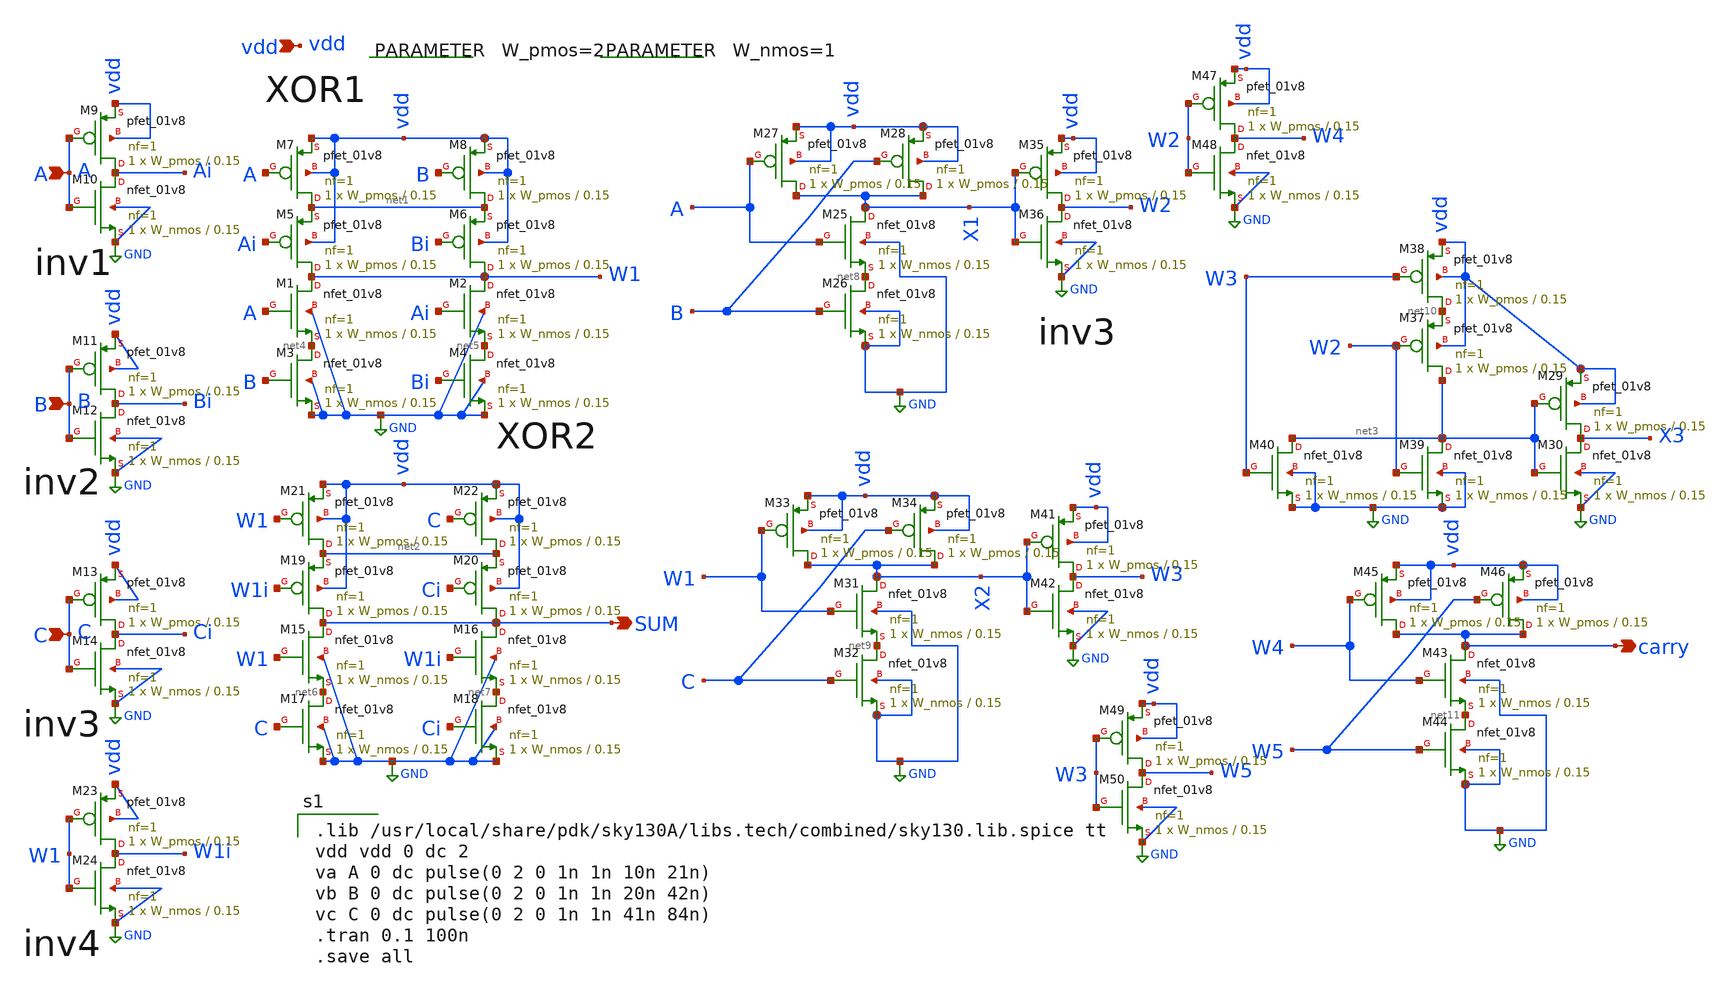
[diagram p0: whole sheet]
** sch_path: Circuit Files/circuits/circuits/FA_mos_realization.sch
**.subckt FA_mos_realization A B vdd C SUM carry
*.ipin A
*.ipin B
*.ipin vdd
*.ipin C
*.opin SUM
*.opin carry
XM1 W1 A net4 GND sky130_fd_pr__nfet_01v8 L=0.15 W=W_nmos nf=1 ad='int((nf+1)/2) * W/nf * 0.29' as='int((nf+2)/2) * W/nf * 0.29'
+ pd='2*int((nf+1)/2) * (W/nf + 0.29)' ps='2*int((nf+2)/2) * (W/nf + 0.29)' nrd='0.29 / W' nrs='0.29 / W'
+ sa=0 sb=0 sd=0 mult=1 m=1
XM2 W1 Ai net5 GND sky130_fd_pr__nfet_01v8 L=0.15 W=W_nmos nf=1 ad='int((nf+1)/2) * W/nf * 0.29' as='int((nf+2)/2) * W/nf * 0.29'
+ pd='2*int((nf+1)/2) * (W/nf + 0.29)' ps='2*int((nf+2)/2) * (W/nf + 0.29)' nrd='0.29 / W' nrs='0.29 / W'
+ sa=0 sb=0 sd=0 mult=1 m=1
XM3 net4 B GND GND sky130_fd_pr__nfet_01v8 L=0.15 W=W_nmos nf=1 ad='int((nf+1)/2) * W/nf * 0.29' as='int((nf+2)/2) * W/nf * 0.29'
+ pd='2*int((nf+1)/2) * (W/nf + 0.29)' ps='2*int((nf+2)/2) * (W/nf + 0.29)' nrd='0.29 / W' nrs='0.29 / W'
+ sa=0 sb=0 sd=0 mult=1 m=1
XM4 net5 Bi GND GND sky130_fd_pr__nfet_01v8 L=0.15 W=W_nmos nf=1 ad='int((nf+1)/2) * W/nf * 0.29' as='int((nf+2)/2) * W/nf * 0.29'
+ pd='2*int((nf+1)/2) * (W/nf + 0.29)' ps='2*int((nf+2)/2) * (W/nf + 0.29)' nrd='0.29 / W' nrs='0.29 / W'
+ sa=0 sb=0 sd=0 mult=1 m=1
XM5 W1 Ai net1 vdd sky130_fd_pr__pfet_01v8 L=0.15 W=W_pmos nf=1 ad='int((nf+1)/2) * W/nf * 0.29' as='int((nf+2)/2) * W/nf * 0.29'
+ pd='2*int((nf+1)/2) * (W/nf + 0.29)' ps='2*int((nf+2)/2) * (W/nf + 0.29)' nrd='0.29 / W' nrs='0.29 / W'
+ sa=0 sb=0 sd=0 mult=1 m=1
XM6 W1 Bi net1 vdd sky130_fd_pr__pfet_01v8 L=0.15 W=W_pmos nf=1 ad='int((nf+1)/2) * W/nf * 0.29' as='int((nf+2)/2) * W/nf * 0.29'
+ pd='2*int((nf+1)/2) * (W/nf + 0.29)' ps='2*int((nf+2)/2) * (W/nf + 0.29)' nrd='0.29 / W' nrs='0.29 / W'
+ sa=0 sb=0 sd=0 mult=1 m=1
XM7 net1 A vdd vdd sky130_fd_pr__pfet_01v8 L=0.15 W=W_pmos nf=1 ad='int((nf+1)/2) * W/nf * 0.29' as='int((nf+2)/2) * W/nf * 0.29'
+ pd='2*int((nf+1)/2) * (W/nf + 0.29)' ps='2*int((nf+2)/2) * (W/nf + 0.29)' nrd='0.29 / W' nrs='0.29 / W'
+ sa=0 sb=0 sd=0 mult=1 m=1
XM8 net1 B vdd vdd sky130_fd_pr__pfet_01v8 L=0.15 W=W_pmos nf=1 ad='int((nf+1)/2) * W/nf * 0.29' as='int((nf+2)/2) * W/nf * 0.29'
+ pd='2*int((nf+1)/2) * (W/nf + 0.29)' ps='2*int((nf+2)/2) * (W/nf + 0.29)' nrd='0.29 / W' nrs='0.29 / W'
+ sa=0 sb=0 sd=0 mult=1 m=1
XM9 Ai A vdd vdd sky130_fd_pr__pfet_01v8 L=0.15 W=W_pmos nf=1 ad='int((nf+1)/2) * W/nf * 0.29' as='int((nf+2)/2) * W/nf * 0.29'
+ pd='2*int((nf+1)/2) * (W/nf + 0.29)' ps='2*int((nf+2)/2) * (W/nf + 0.29)' nrd='0.29 / W' nrs='0.29 / W'
+ sa=0 sb=0 sd=0 mult=1 m=1
XM10 Ai A GND GND sky130_fd_pr__nfet_01v8 L=0.15 W=W_nmos nf=1 ad='int((nf+1)/2) * W/nf * 0.29' as='int((nf+2)/2) * W/nf * 0.29'
+ pd='2*int((nf+1)/2) * (W/nf + 0.29)' ps='2*int((nf+2)/2) * (W/nf + 0.29)' nrd='0.29 / W' nrs='0.29 / W'
+ sa=0 sb=0 sd=0 mult=1 m=1
XM11 Bi B vdd vdd sky130_fd_pr__pfet_01v8 L=0.15 W=W_pmos nf=1 ad='int((nf+1)/2) * W/nf * 0.29' as='int((nf+2)/2) * W/nf * 0.29'
+ pd='2*int((nf+1)/2) * (W/nf + 0.29)' ps='2*int((nf+2)/2) * (W/nf + 0.29)' nrd='0.29 / W' nrs='0.29 / W'
+ sa=0 sb=0 sd=0 mult=1 m=1
XM12 Bi B GND GND sky130_fd_pr__nfet_01v8 L=0.15 W=W_nmos nf=1 ad='int((nf+1)/2) * W/nf * 0.29' as='int((nf+2)/2) * W/nf * 0.29'
+ pd='2*int((nf+1)/2) * (W/nf + 0.29)' ps='2*int((nf+2)/2) * (W/nf + 0.29)' nrd='0.29 / W' nrs='0.29 / W'
+ sa=0 sb=0 sd=0 mult=1 m=1
XM13 Ci C vdd vdd sky130_fd_pr__pfet_01v8 L=0.15 W=W_pmos nf=1 ad='int((nf+1)/2) * W/nf * 0.29' as='int((nf+2)/2) * W/nf * 0.29'
+ pd='2*int((nf+1)/2) * (W/nf + 0.29)' ps='2*int((nf+2)/2) * (W/nf + 0.29)' nrd='0.29 / W' nrs='0.29 / W'
+ sa=0 sb=0 sd=0 mult=1 m=1
XM14 Ci C GND GND sky130_fd_pr__nfet_01v8 L=0.15 W=W_nmos nf=1 ad='int((nf+1)/2) * W/nf * 0.29' as='int((nf+2)/2) * W/nf * 0.29'
+ pd='2*int((nf+1)/2) * (W/nf + 0.29)' ps='2*int((nf+2)/2) * (W/nf + 0.29)' nrd='0.29 / W' nrs='0.29 / W'
+ sa=0 sb=0 sd=0 mult=1 m=1
XM15 SUM W1 net6 GND sky130_fd_pr__nfet_01v8 L=0.15 W=W_nmos nf=1 ad='int((nf+1)/2) * W/nf * 0.29' as='int((nf+2)/2) * W/nf * 0.29'
+ pd='2*int((nf+1)/2) * (W/nf + 0.29)' ps='2*int((nf+2)/2) * (W/nf + 0.29)' nrd='0.29 / W' nrs='0.29 / W'
+ sa=0 sb=0 sd=0 mult=1 m=1
XM16 SUM W1i net7 GND sky130_fd_pr__nfet_01v8 L=0.15 W=W_nmos nf=1 ad='int((nf+1)/2) * W/nf * 0.29' as='int((nf+2)/2) * W/nf * 0.29'
+ pd='2*int((nf+1)/2) * (W/nf + 0.29)' ps='2*int((nf+2)/2) * (W/nf + 0.29)' nrd='0.29 / W' nrs='0.29 / W'
+ sa=0 sb=0 sd=0 mult=1 m=1
XM17 net6 C GND GND sky130_fd_pr__nfet_01v8 L=0.15 W=W_nmos nf=1 ad='int((nf+1)/2) * W/nf * 0.29' as='int((nf+2)/2) * W/nf * 0.29'
+ pd='2*int((nf+1)/2) * (W/nf + 0.29)' ps='2*int((nf+2)/2) * (W/nf + 0.29)' nrd='0.29 / W' nrs='0.29 / W'
+ sa=0 sb=0 sd=0 mult=1 m=1
XM18 net7 Ci GND GND sky130_fd_pr__nfet_01v8 L=0.15 W=W_nmos nf=1 ad='int((nf+1)/2) * W/nf * 0.29' as='int((nf+2)/2) * W/nf * 0.29'
+ pd='2*int((nf+1)/2) * (W/nf + 0.29)' ps='2*int((nf+2)/2) * (W/nf + 0.29)' nrd='0.29 / W' nrs='0.29 / W'
+ sa=0 sb=0 sd=0 mult=1 m=1
XM19 SUM W1i net2 vdd sky130_fd_pr__pfet_01v8 L=0.15 W=W_pmos nf=1 ad='int((nf+1)/2) * W/nf * 0.29' as='int((nf+2)/2) * W/nf * 0.29'
+ pd='2*int((nf+1)/2) * (W/nf + 0.29)' ps='2*int((nf+2)/2) * (W/nf + 0.29)' nrd='0.29 / W' nrs='0.29 / W'
+ sa=0 sb=0 sd=0 mult=1 m=1
XM20 SUM Ci net2 vdd sky130_fd_pr__pfet_01v8 L=0.15 W=W_pmos nf=1 ad='int((nf+1)/2) * W/nf * 0.29' as='int((nf+2)/2) * W/nf * 0.29'
+ pd='2*int((nf+1)/2) * (W/nf + 0.29)' ps='2*int((nf+2)/2) * (W/nf + 0.29)' nrd='0.29 / W' nrs='0.29 / W'
+ sa=0 sb=0 sd=0 mult=1 m=1
XM21 net2 W1 vdd vdd sky130_fd_pr__pfet_01v8 L=0.15 W=W_pmos nf=1 ad='int((nf+1)/2) * W/nf * 0.29' as='int((nf+2)/2) * W/nf * 0.29'
+ pd='2*int((nf+1)/2) * (W/nf + 0.29)' ps='2*int((nf+2)/2) * (W/nf + 0.29)' nrd='0.29 / W' nrs='0.29 / W'
+ sa=0 sb=0 sd=0 mult=1 m=1
XM22 net2 C vdd vdd sky130_fd_pr__pfet_01v8 L=0.15 W=W_pmos nf=1 ad='int((nf+1)/2) * W/nf * 0.29' as='int((nf+2)/2) * W/nf * 0.29'
+ pd='2*int((nf+1)/2) * (W/nf + 0.29)' ps='2*int((nf+2)/2) * (W/nf + 0.29)' nrd='0.29 / W' nrs='0.29 / W'
+ sa=0 sb=0 sd=0 mult=1 m=1
XM23 W1i W1 vdd vdd sky130_fd_pr__pfet_01v8 L=0.15 W=W_pmos nf=1 ad='int((nf+1)/2) * W/nf * 0.29' as='int((nf+2)/2) * W/nf * 0.29'
+ pd='2*int((nf+1)/2) * (W/nf + 0.29)' ps='2*int((nf+2)/2) * (W/nf + 0.29)' nrd='0.29 / W' nrs='0.29 / W'
+ sa=0 sb=0 sd=0 mult=1 m=1
XM24 W1i W1 GND GND sky130_fd_pr__nfet_01v8 L=0.15 W=W_nmos nf=1 ad='int((nf+1)/2) * W/nf * 0.29' as='int((nf+2)/2) * W/nf * 0.29'
+ pd='2*int((nf+1)/2) * (W/nf + 0.29)' ps='2*int((nf+2)/2) * (W/nf + 0.29)' nrd='0.29 / W' nrs='0.29 / W'
+ sa=0 sb=0 sd=0 mult=1 m=1
XM25 X1 A net8 GND sky130_fd_pr__nfet_01v8 L=0.15 W=W_nmos nf=1 ad='int((nf+1)/2) * W/nf * 0.29' as='int((nf+2)/2) * W/nf * 0.29'
+ pd='2*int((nf+1)/2) * (W/nf + 0.29)' ps='2*int((nf+2)/2) * (W/nf + 0.29)' nrd='0.29 / W' nrs='0.29 / W'
+ sa=0 sb=0 sd=0 mult=1 m=1
XM26 net8 B GND GND sky130_fd_pr__nfet_01v8 L=0.15 W=W_nmos nf=1 ad='int((nf+1)/2) * W/nf * 0.29' as='int((nf+2)/2) * W/nf * 0.29'
+ pd='2*int((nf+1)/2) * (W/nf + 0.29)' ps='2*int((nf+2)/2) * (W/nf + 0.29)' nrd='0.29 / W' nrs='0.29 / W'
+ sa=0 sb=0 sd=0 mult=1 m=1
XM27 X1 A vdd vdd sky130_fd_pr__pfet_01v8 L=0.15 W=W_pmos nf=1 ad='int((nf+1)/2) * W/nf * 0.29' as='int((nf+2)/2) * W/nf * 0.29'
+ pd='2*int((nf+1)/2) * (W/nf + 0.29)' ps='2*int((nf+2)/2) * (W/nf + 0.29)' nrd='0.29 / W' nrs='0.29 / W'
+ sa=0 sb=0 sd=0 mult=1 m=1
XM28 X1 B vdd vdd sky130_fd_pr__pfet_01v8 L=0.15 W=W_pmos nf=1 ad='int((nf+1)/2) * W/nf * 0.29' as='int((nf+2)/2) * W/nf * 0.29'
+ pd='2*int((nf+1)/2) * (W/nf + 0.29)' ps='2*int((nf+2)/2) * (W/nf + 0.29)' nrd='0.29 / W' nrs='0.29 / W'
+ sa=0 sb=0 sd=0 mult=1 m=1
XM31 X2 W1 net9 GND sky130_fd_pr__nfet_01v8 L=0.15 W=W_nmos nf=1 ad='int((nf+1)/2) * W/nf * 0.29' as='int((nf+2)/2) * W/nf * 0.29'
+ pd='2*int((nf+1)/2) * (W/nf + 0.29)' ps='2*int((nf+2)/2) * (W/nf + 0.29)' nrd='0.29 / W' nrs='0.29 / W'
+ sa=0 sb=0 sd=0 mult=1 m=1
XM32 net9 C GND GND sky130_fd_pr__nfet_01v8 L=0.15 W=W_nmos nf=1 ad='int((nf+1)/2) * W/nf * 0.29' as='int((nf+2)/2) * W/nf * 0.29'
+ pd='2*int((nf+1)/2) * (W/nf + 0.29)' ps='2*int((nf+2)/2) * (W/nf + 0.29)' nrd='0.29 / W' nrs='0.29 / W'
+ sa=0 sb=0 sd=0 mult=1 m=1
XM33 X2 W1 vdd vdd sky130_fd_pr__pfet_01v8 L=0.15 W=W_pmos nf=1 ad='int((nf+1)/2) * W/nf * 0.29' as='int((nf+2)/2) * W/nf * 0.29'
+ pd='2*int((nf+1)/2) * (W/nf + 0.29)' ps='2*int((nf+2)/2) * (W/nf + 0.29)' nrd='0.29 / W' nrs='0.29 / W'
+ sa=0 sb=0 sd=0 mult=1 m=1
XM34 X2 C vdd vdd sky130_fd_pr__pfet_01v8 L=0.15 W=W_pmos nf=1 ad='int((nf+1)/2) * W/nf * 0.29' as='int((nf+2)/2) * W/nf * 0.29'
+ pd='2*int((nf+1)/2) * (W/nf + 0.29)' ps='2*int((nf+2)/2) * (W/nf + 0.29)' nrd='0.29 / W' nrs='0.29 / W'
+ sa=0 sb=0 sd=0 mult=1 m=1
XM37 net3 W2 net10 vdd sky130_fd_pr__pfet_01v8 L=0.15 W=W_pmos nf=1 ad='int((nf+1)/2) * W/nf * 0.29'
+ as='int((nf+2)/2) * W/nf * 0.29' pd='2*int((nf+1)/2) * (W/nf + 0.29)' ps='2*int((nf+2)/2) * (W/nf + 0.29)'
+ nrd='0.29 / W' nrs='0.29 / W' sa=0 sb=0 sd=0 mult=1 m=1
XM38 net10 W3 vdd vdd sky130_fd_pr__pfet_01v8 L=0.15 W=W_pmos nf=1 ad='int((nf+1)/2) * W/nf * 0.29' as='int((nf+2)/2) * W/nf * 0.29'
+ pd='2*int((nf+1)/2) * (W/nf + 0.29)' ps='2*int((nf+2)/2) * (W/nf + 0.29)' nrd='0.29 / W' nrs='0.29 / W'
+ sa=0 sb=0 sd=0 mult=1 m=1
XM39 net3 W2 GND GND sky130_fd_pr__nfet_01v8 L=0.15 W=W_nmos nf=1 ad='int((nf+1)/2) * W/nf * 0.29' as='int((nf+2)/2) * W/nf * 0.29'
+ pd='2*int((nf+1)/2) * (W/nf + 0.29)' ps='2*int((nf+2)/2) * (W/nf + 0.29)' nrd='0.29 / W' nrs='0.29 / W'
+ sa=0 sb=0 sd=0 mult=1 m=1
XM40 net3 W3 GND GND sky130_fd_pr__nfet_01v8 L=0.15 W=W_nmos nf=1 ad='int((nf+1)/2) * W/nf * 0.29' as='int((nf+2)/2) * W/nf * 0.29'
+ pd='2*int((nf+1)/2) * (W/nf + 0.29)' ps='2*int((nf+2)/2) * (W/nf + 0.29)' nrd='0.29 / W' nrs='0.29 / W'
+ sa=0 sb=0 sd=0 mult=1 m=1
XM29 X3 net3 vdd vdd sky130_fd_pr__pfet_01v8 L=0.15 W=W_pmos nf=1 ad='int((nf+1)/2) * W/nf * 0.29' as='int((nf+2)/2) * W/nf * 0.29'
+ pd='2*int((nf+1)/2) * (W/nf + 0.29)' ps='2*int((nf+2)/2) * (W/nf + 0.29)' nrd='0.29 / W' nrs='0.29 / W'
+ sa=0 sb=0 sd=0 mult=1 m=1
XM30 X3 net3 GND GND sky130_fd_pr__nfet_01v8 L=0.15 W=W_nmos nf=1 ad='int((nf+1)/2) * W/nf * 0.29' as='int((nf+2)/2) * W/nf * 0.29'
+ pd='2*int((nf+1)/2) * (W/nf + 0.29)' ps='2*int((nf+2)/2) * (W/nf + 0.29)' nrd='0.29 / W' nrs='0.29 / W'
+ sa=0 sb=0 sd=0 mult=1 m=1
XM35 W2 X1 vdd vdd sky130_fd_pr__pfet_01v8 L=0.15 W=W_pmos nf=1 ad='int((nf+1)/2) * W/nf * 0.29' as='int((nf+2)/2) * W/nf * 0.29'
+ pd='2*int((nf+1)/2) * (W/nf + 0.29)' ps='2*int((nf+2)/2) * (W/nf + 0.29)' nrd='0.29 / W' nrs='0.29 / W'
+ sa=0 sb=0 sd=0 mult=1 m=1
XM36 W2 X1 GND GND sky130_fd_pr__nfet_01v8 L=0.15 W=W_nmos nf=1 ad='int((nf+1)/2) * W/nf * 0.29' as='int((nf+2)/2) * W/nf * 0.29'
+ pd='2*int((nf+1)/2) * (W/nf + 0.29)' ps='2*int((nf+2)/2) * (W/nf + 0.29)' nrd='0.29 / W' nrs='0.29 / W'
+ sa=0 sb=0 sd=0 mult=1 m=1
XM41 W3 X2 vdd vdd sky130_fd_pr__pfet_01v8 L=0.15 W=W_pmos nf=1 ad='int((nf+1)/2) * W/nf * 0.29' as='int((nf+2)/2) * W/nf * 0.29'
+ pd='2*int((nf+1)/2) * (W/nf + 0.29)' ps='2*int((nf+2)/2) * (W/nf + 0.29)' nrd='0.29 / W' nrs='0.29 / W'
+ sa=0 sb=0 sd=0 mult=1 m=1
XM42 W3 X2 GND GND sky130_fd_pr__nfet_01v8 L=0.15 W=W_nmos nf=1 ad='int((nf+1)/2) * W/nf * 0.29' as='int((nf+2)/2) * W/nf * 0.29'
+ pd='2*int((nf+1)/2) * (W/nf + 0.29)' ps='2*int((nf+2)/2) * (W/nf + 0.29)' nrd='0.29 / W' nrs='0.29 / W'
+ sa=0 sb=0 sd=0 mult=1 m=1
XM43 carry W4 net11 GND sky130_fd_pr__nfet_01v8 L=0.15 W=W_nmos nf=1 ad='int((nf+1)/2) * W/nf * 0.29'
+ as='int((nf+2)/2) * W/nf * 0.29' pd='2*int((nf+1)/2) * (W/nf + 0.29)' ps='2*int((nf+2)/2) * (W/nf + 0.29)'
+ nrd='0.29 / W' nrs='0.29 / W' sa=0 sb=0 sd=0 mult=1 m=1
XM44 net11 W5 GND GND sky130_fd_pr__nfet_01v8 L=0.15 W=W_nmos nf=1 ad='int((nf+1)/2) * W/nf * 0.29' as='int((nf+2)/2) * W/nf * 0.29'
+ pd='2*int((nf+1)/2) * (W/nf + 0.29)' ps='2*int((nf+2)/2) * (W/nf + 0.29)' nrd='0.29 / W' nrs='0.29 / W'
+ sa=0 sb=0 sd=0 mult=1 m=1
XM45 carry W4 vdd vdd sky130_fd_pr__pfet_01v8 L=0.15 W=W_pmos nf=1 ad='int((nf+1)/2) * W/nf * 0.29' as='int((nf+2)/2) * W/nf * 0.29'
+ pd='2*int((nf+1)/2) * (W/nf + 0.29)' ps='2*int((nf+2)/2) * (W/nf + 0.29)' nrd='0.29 / W' nrs='0.29 / W'
+ sa=0 sb=0 sd=0 mult=1 m=1
XM46 carry W5 vdd vdd sky130_fd_pr__pfet_01v8 L=0.15 W=W_pmos nf=1 ad='int((nf+1)/2) * W/nf * 0.29' as='int((nf+2)/2) * W/nf * 0.29'
+ pd='2*int((nf+1)/2) * (W/nf + 0.29)' ps='2*int((nf+2)/2) * (W/nf + 0.29)' nrd='0.29 / W' nrs='0.29 / W'
+ sa=0 sb=0 sd=0 mult=1 m=1
.param W_pmos=2
.param W_nmos=1
XM47 W4 W2 vdd vdd sky130_fd_pr__pfet_01v8 L=0.15 W=W_pmos nf=1 ad='int((nf+1)/2) * W/nf * 0.29' as='int((nf+2)/2) * W/nf * 0.29'
+ pd='2*int((nf+1)/2) * (W/nf + 0.29)' ps='2*int((nf+2)/2) * (W/nf + 0.29)' nrd='0.29 / W' nrs='0.29 / W'
+ sa=0 sb=0 sd=0 mult=1 m=1
XM48 W4 W2 GND GND sky130_fd_pr__nfet_01v8 L=0.15 W=W_nmos nf=1 ad='int((nf+1)/2) * W/nf * 0.29' as='int((nf+2)/2) * W/nf * 0.29'
+ pd='2*int((nf+1)/2) * (W/nf + 0.29)' ps='2*int((nf+2)/2) * (W/nf + 0.29)' nrd='0.29 / W' nrs='0.29 / W'
+ sa=0 sb=0 sd=0 mult=1 m=1
XM49 W5 W3 vdd vdd sky130_fd_pr__pfet_01v8 L=0.15 W=W_pmos nf=1 ad='int((nf+1)/2) * W/nf * 0.29' as='int((nf+2)/2) * W/nf * 0.29'
+ pd='2*int((nf+1)/2) * (W/nf + 0.29)' ps='2*int((nf+2)/2) * (W/nf + 0.29)' nrd='0.29 / W' nrs='0.29 / W'
+ sa=0 sb=0 sd=0 mult=1 m=1
XM50 W5 W3 GND GND sky130_fd_pr__nfet_01v8 L=0.15 W=W_nmos nf=1 ad='int((nf+1)/2) * W/nf * 0.29' as='int((nf+2)/2) * W/nf * 0.29'
+ pd='2*int((nf+1)/2) * (W/nf + 0.29)' ps='2*int((nf+2)/2) * (W/nf + 0.29)' nrd='0.29 / W' nrs='0.29 / W'
+ sa=0 sb=0 sd=0 mult=1 m=1
**** begin user architecture code

.lib /usr/local/share/pdk/sky130A/libs.tech/combined/sky130.lib.spice tt
vdd vdd 0 dc 2
va A 0 dc pulse(0 2 0 1n 1n 10n 21n)
vb B 0 dc pulse(0 2 0 1n 1n 20n 42n)
vc C 0 dc pulse(0 2 0 1n 1n 41n 84n)
.tran 0.1 100n
.save all

**** end user architecture code
**.ends
.GLOBAL GND
.end
